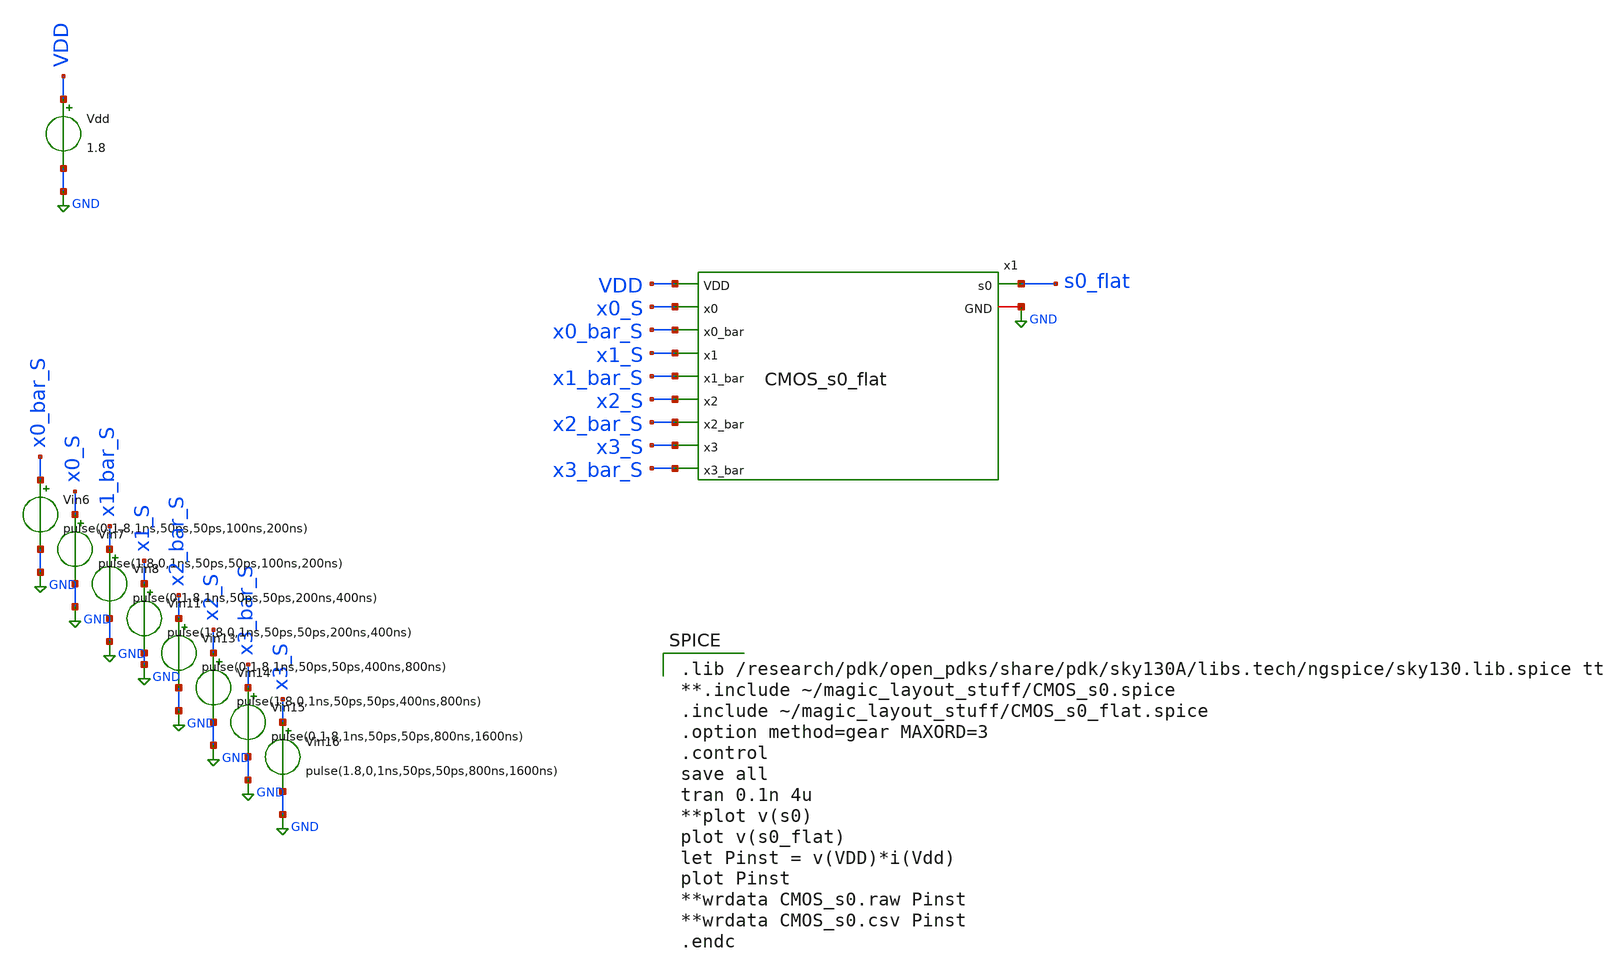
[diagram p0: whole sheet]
** sch_path: skywater_stuff/CMOS_s0_sim.sch
**.subckt CMOS_s0_sim
Vdd VDD GND 1.8
Vin6 x0_bar_S GND pulse(0,1.8,1ns,50ps,50ps,100ns,200ns)
Vin7 x0_S GND pulse(1.8,0,1ns,50ps,50ps,100ns,200ns)
Vin8 x1_bar_S GND pulse(0,1.8,1ns,50ps,50ps,200ns,400ns)
Vin11 x1_S GND pulse(1.8,0,1ns,50ps,50ps,200ns,400ns)
Vin13 x2_bar_S GND pulse(0,1.8,1ns,50ps,50ps,400ns,800ns)
Vin14 x2_S GND pulse(1.8,0,1ns,50ps,50ps,400ns,800ns)
Vin15 x3_bar_S GND pulse(0,1.8,1ns,50ps,50ps,800ns,1600ns)
Vin16 x3_S GND pulse(1.8,0,1ns,50ps,50ps,800ns,1600ns)
x1 GND x0_S x0_bar_S x1_S x1_bar_S x2_S x2_bar_S x3_S x3_bar_S s0_flat VDD CMOS_s0_flat
**** begin user architecture code

.lib /research/pdk/open_pdks/share/pdk/sky130A/libs.tech/ngspice/sky130.lib.spice tt
**.include ~/magic_layout_stuff/CMOS_s0.spice
.include ~/magic_layout_stuff/CMOS_s0_flat.spice
.option method=gear MAXORD=3
.control
save all
tran 0.1n 4u
**plot v(s0)
plot v(s0_flat)
let Pinst = v(VDD)*i(Vdd)
plot Pinst
**wrdata CMOS_s0.raw Pinst
**wrdata CMOS_s0.csv Pinst
.endc


**** end user architecture code
**.ends
.GLOBAL GND
.end
